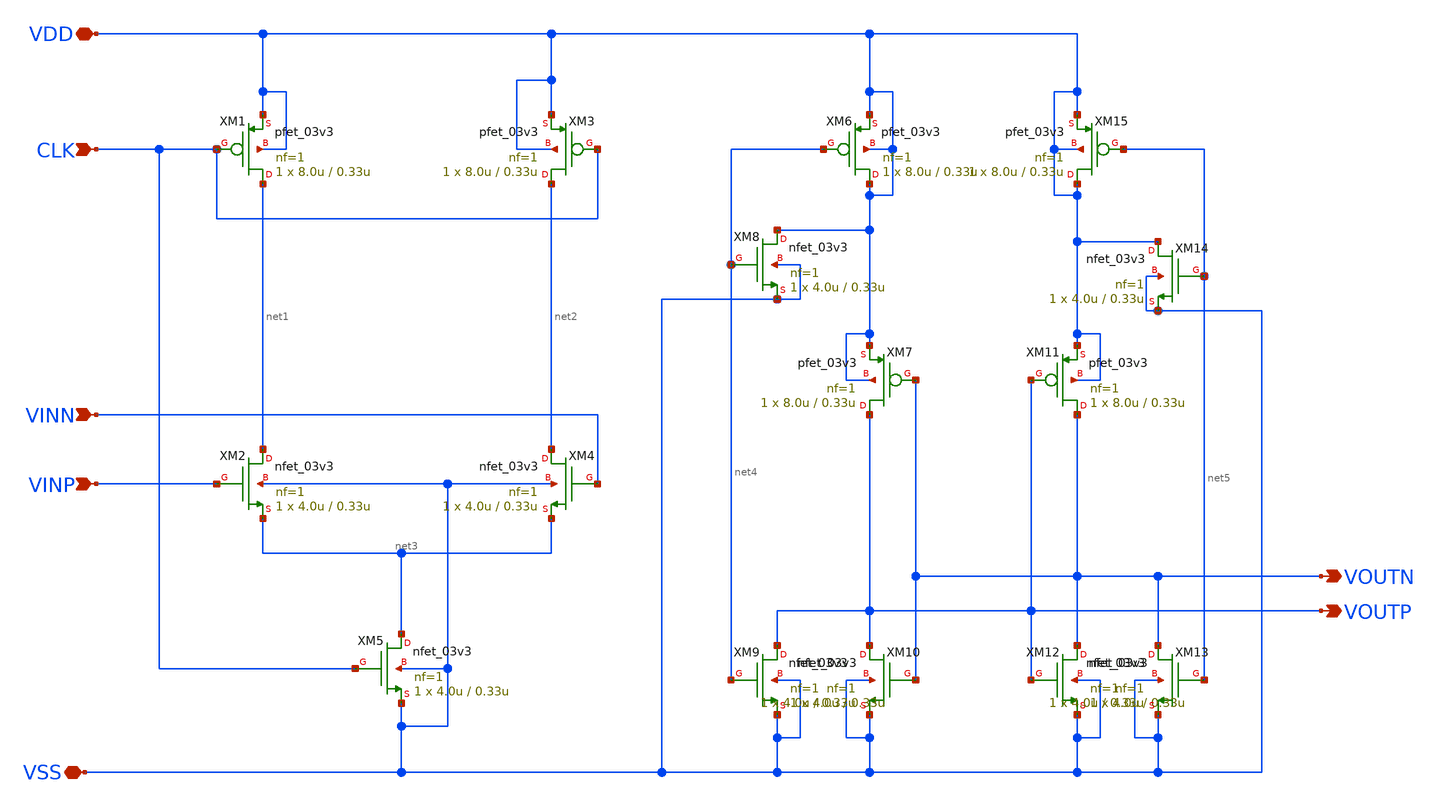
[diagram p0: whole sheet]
** sch_path: noritsuna/comparator/comparator.sch
**.subckt comparator VINN VDD VSS VOUTN VOUTP CLK VINP
*.ipin VINN
*.iopin VDD
*.iopin VSS
*.opin VOUTN
*.opin VOUTP
*.ipin CLK
*.ipin VINP
XM1 net1 CLK VDD VDD pfet_03v3 L=0.33u W=8.0u nf=1 ad='int((nf+1)/2) * W/nf * 0.18u' as='int((nf+2)/2) * W/nf * 0.18u'
+ pd='2*int((nf+1)/2) * (W/nf + 0.18u)' ps='2*int((nf+2)/2) * (W/nf + 0.18u)' nrd='0.18u / W' nrs='0.18u / W'
+ sa=0 sb=0 sd=0 m=1
XM2 net1 VINP net3 VSS nfet_03v3 L=0.33u W=4.0u nf=1 ad='int((nf+1)/2) * W/nf * 0.18u' as='int((nf+2)/2) * W/nf * 0.18u'
+ pd='2*int((nf+1)/2) * (W/nf + 0.18u)' ps='2*int((nf+2)/2) * (W/nf + 0.18u)' nrd='0.18u / W' nrs='0.18u / W'
+ sa=0 sb=0 sd=0 m=1
XM3 net2 CLK VDD VDD pfet_03v3 L=0.33u W=8.0u nf=1 ad='int((nf+1)/2) * W/nf * 0.18u' as='int((nf+2)/2) * W/nf * 0.18u'
+ pd='2*int((nf+1)/2) * (W/nf + 0.18u)' ps='2*int((nf+2)/2) * (W/nf + 0.18u)' nrd='0.18u / W' nrs='0.18u / W'
+ sa=0 sb=0 sd=0 m=1
XM4 net2 VINN net3 VSS nfet_03v3 L=0.33u W=4.0u nf=1 ad='int((nf+1)/2) * W/nf * 0.18u' as='int((nf+2)/2) * W/nf * 0.18u'
+ pd='2*int((nf+1)/2) * (W/nf + 0.18u)' ps='2*int((nf+2)/2) * (W/nf + 0.18u)' nrd='0.18u / W' nrs='0.18u / W'
+ sa=0 sb=0 sd=0 m=1
XM5 net3 CLK VSS VSS nfet_03v3 L=0.33u W=4.0u nf=1 ad='int((nf+1)/2) * W/nf * 0.18u' as='int((nf+2)/2) * W/nf * 0.18u'
+ pd='2*int((nf+1)/2) * (W/nf + 0.18u)' ps='2*int((nf+2)/2) * (W/nf + 0.18u)' nrd='0.18u / W' nrs='0.18u / W'
+ sa=0 sb=0 sd=0 m=1
XM6 VDD net4 VDD VDD pfet_03v3 L=0.33u W=8.0u nf=1 ad='int((nf+1)/2) * W/nf * 0.18u' as='int((nf+2)/2) * W/nf * 0.18u'
+ pd='2*int((nf+1)/2) * (W/nf + 0.18u)' ps='2*int((nf+2)/2) * (W/nf + 0.18u)' nrd='0.18u / W' nrs='0.18u / W'
+ sa=0 sb=0 sd=0 m=1
XM7 VOUTP VOUTN VDD VDD pfet_03v3 L=0.33u W=8.0u nf=1 ad='int((nf+1)/2) * W/nf * 0.18u' as='int((nf+2)/2) * W/nf * 0.18u'
+ pd='2*int((nf+1)/2) * (W/nf + 0.18u)' ps='2*int((nf+2)/2) * (W/nf + 0.18u)' nrd='0.18u / W' nrs='0.18u / W'
+ sa=0 sb=0 sd=0 m=1
XM8 VDD net4 VSS VSS nfet_03v3 L=0.33u W=4.0u nf=1 ad='int((nf+1)/2) * W/nf * 0.18u' as='int((nf+2)/2) * W/nf * 0.18u'
+ pd='2*int((nf+1)/2) * (W/nf + 0.18u)' ps='2*int((nf+2)/2) * (W/nf + 0.18u)' nrd='0.18u / W' nrs='0.18u / W'
+ sa=0 sb=0 sd=0 m=1
XM9 VOUTP net4 VSS VSS nfet_03v3 L=0.33u W=4.0u nf=1 ad='int((nf+1)/2) * W/nf * 0.18u' as='int((nf+2)/2) * W/nf * 0.18u'
+ pd='2*int((nf+1)/2) * (W/nf + 0.18u)' ps='2*int((nf+2)/2) * (W/nf + 0.18u)' nrd='0.18u / W' nrs='0.18u / W'
+ sa=0 sb=0 sd=0 m=1
XM10 VOUTP VOUTN VSS VSS nfet_03v3 L=0.33u W=4.0u nf=1 ad='int((nf+1)/2) * W/nf * 0.18u' as='int((nf+2)/2) * W/nf * 0.18u'
+ pd='2*int((nf+1)/2) * (W/nf + 0.18u)' ps='2*int((nf+2)/2) * (W/nf + 0.18u)' nrd='0.18u / W' nrs='0.18u / W'
+ sa=0 sb=0 sd=0 m=1
XM11 VOUTN VOUTP VDD VDD pfet_03v3 L=0.33u W=8.0u nf=1 ad='int((nf+1)/2) * W/nf * 0.18u' as='int((nf+2)/2) * W/nf * 0.18u'
+ pd='2*int((nf+1)/2) * (W/nf + 0.18u)' ps='2*int((nf+2)/2) * (W/nf + 0.18u)' nrd='0.18u / W' nrs='0.18u / W'
+ sa=0 sb=0 sd=0 m=1
XM12 VOUTN VOUTP VSS VSS nfet_03v3 L=0.33u W=4.0u nf=1 ad='int((nf+1)/2) * W/nf * 0.18u' as='int((nf+2)/2) * W/nf * 0.18u'
+ pd='2*int((nf+1)/2) * (W/nf + 0.18u)' ps='2*int((nf+2)/2) * (W/nf + 0.18u)' nrd='0.18u / W' nrs='0.18u / W'
+ sa=0 sb=0 sd=0 m=1
XM13 VOUTN net5 VSS VSS nfet_03v3 L=0.33u W=4.0u nf=1 ad='int((nf+1)/2) * W/nf * 0.18u' as='int((nf+2)/2) * W/nf * 0.18u'
+ pd='2*int((nf+1)/2) * (W/nf + 0.18u)' ps='2*int((nf+2)/2) * (W/nf + 0.18u)' nrd='0.18u / W' nrs='0.18u / W'
+ sa=0 sb=0 sd=0 m=1
XM14 VDD net5 VSS VSS nfet_03v3 L=0.33u W=4.0u nf=1 ad='int((nf+1)/2) * W/nf * 0.18u' as='int((nf+2)/2) * W/nf * 0.18u'
+ pd='2*int((nf+1)/2) * (W/nf + 0.18u)' ps='2*int((nf+2)/2) * (W/nf + 0.18u)' nrd='0.18u / W' nrs='0.18u / W'
+ sa=0 sb=0 sd=0 m=1
XM15 VDD net5 VDD VDD pfet_03v3 L=0.33u W=8.0u nf=1 ad='int((nf+1)/2) * W/nf * 0.18u' as='int((nf+2)/2) * W/nf * 0.18u'
+ pd='2*int((nf+1)/2) * (W/nf + 0.18u)' ps='2*int((nf+2)/2) * (W/nf + 0.18u)' nrd='0.18u / W' nrs='0.18u / W'
+ sa=0 sb=0 sd=0 m=1
**.ends
.end
